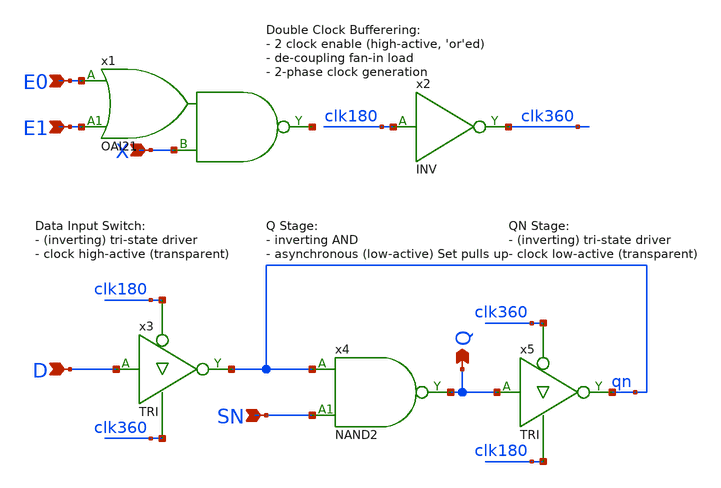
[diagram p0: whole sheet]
** sch_path: Sources/crafted/LATPEES.sch
**.subckt LATPEES X D Q E0 E1 SN
*.ipin X
*.ipin D
*.opin Q
*.ipin E0
*.ipin E1
*.ipin SN
x1 E0 E1 X net1 VDD GND OAI21 Wmin=1.5u Lmin=1u g=2 m=1
x2 clk180 clk360 VDD GND INV Wmin=1.5u Lmin=1u g=2 m=1
x3 D clk180 clk360 qn VDD GND TRI Wmin=1.5u Lmin=1u g=2 m=1
x5 Q clk360 clk180 qn VDD GND TRI Wmin=1.5u Lmin=1u g=2 m=1
x4 qn SN Q VDD GND NAND2 Wmin=1.5u Lmin=1u g=2 m=1
**.ends
.end
